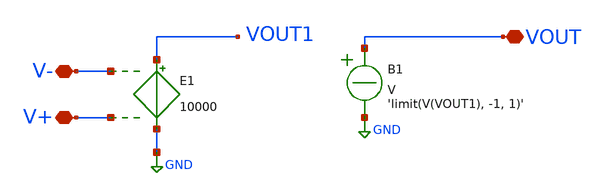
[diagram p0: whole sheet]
** sch_path: Design/Idead_opamp.sch
**.subckt Idead_opamp V- V+ VOUT
*.iopin V-
*.iopin V+
*.iopin VOUT
E1 VOUT1 GND V- V+ 10000
B1 VOUT GND V = 'limit(V(VOUT1), -1, 1)'
**.ends
.GLOBAL GND
.end
